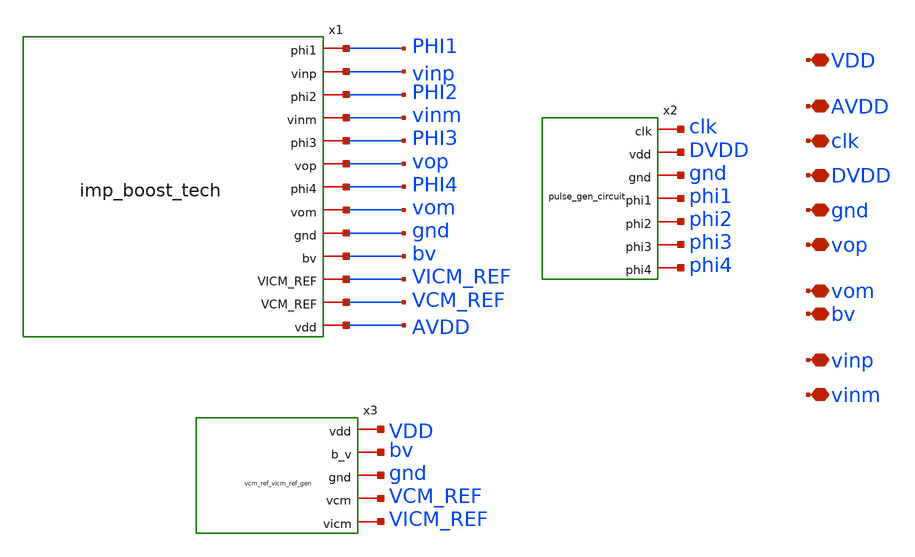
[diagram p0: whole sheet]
** sch_path: dependencies/OTA/dependencies/OTA5174-main/schematic/xschem/digital_pulse_ina_temp_TOP.sch
**.subckt digital_pulse_ina_temp_TOP clk DVDD gnd vop vom bv vinp vinm AVDD VDD
*.iopin clk
*.iopin DVDD
*.iopin gnd
*.iopin vop
*.iopin vom
*.iopin bv
*.iopin vinp
*.iopin vinm
*.iopin AVDD
*.iopin VDD
x1 PHI1 vinp PHI2 vinm PHI3 vop PHI4 vom gnd bv VICM_REF VCM_REF AVDD imp_boost_tech
x2 clk DVDD gnd phi1 phi2 phi3 phi4 pulse_gen_circuit
x3 VDD bv gnd VCM_REF VICM_REF vcm_ref_vicm_ref_gen
**.ends
.end
